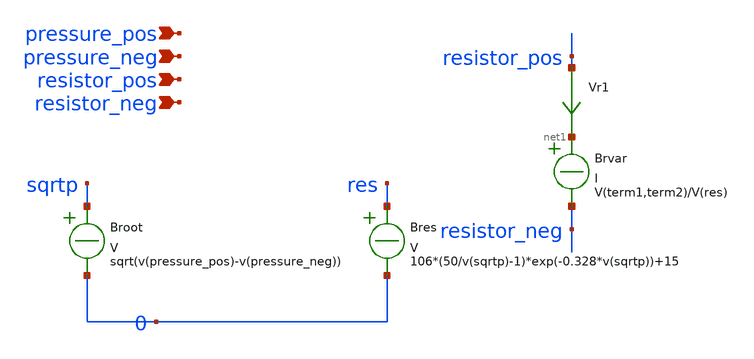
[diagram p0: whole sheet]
** sch_path: piezoresistor.sch
* Copyright 2020 Stefan Frederik Schippers
* Licensed under the Apache License, Version 2.0 (the "License");
* you may not use this file except in compliance with the License.
* You may obtain a copy of the License at
* https://www.apache.org/licenses/LICENSE-2.0
* Unless required by applicable law or agreed to in writing, software
* distributed under the License is distributed on an "AS IS" BASIS,
* WITHOUT WARRANTIES OR CONDITIONS OF ANY KIND, either express or implied.
* See the License for the specific language governing permissions and
* limitations under the License.
**.subckt piezoresistor pressure_pos pressure_neg resistor_pos resistor_neg
*.ipin pressure_pos
*.ipin pressure_neg
*.ipin resistor_pos
*.ipin resistor_neg
Broot sqrtp 0 V = sqrt(v(pressure_pos)-v(pressure_neg))
Bres res 0 V = 106*(50/v(sqrtp)-1)*exp(-0.328*v(sqrtp))+15
Brvar net1 resistor_neg I = V(term1,term2)/V(res)
Vr1 resistor_pos net1 0
.save i(vr1)
**.ends
.end
